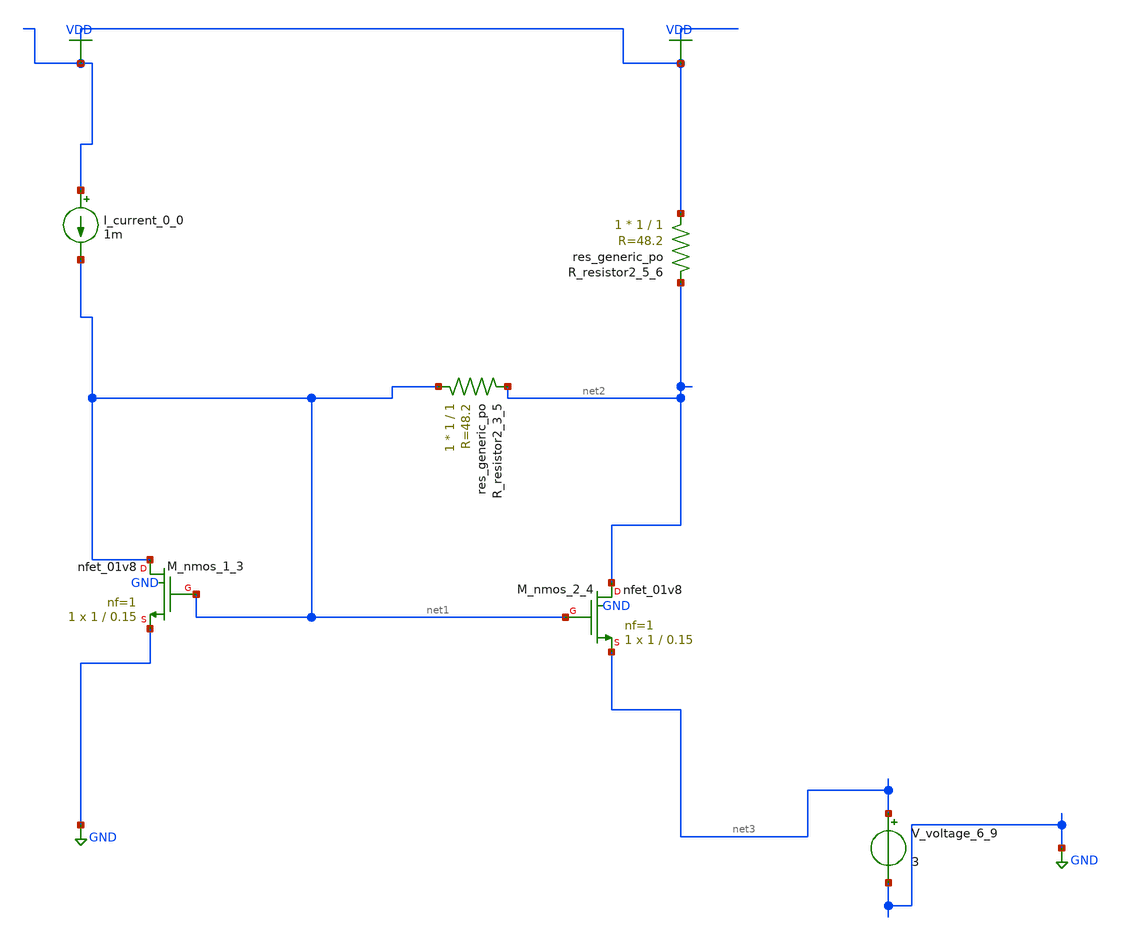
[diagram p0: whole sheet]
** sch_path: schematics/AMSNet/330.sch
**.subckt 330
I_current_0_0 VDD net1 1m
XM_nmos_1_3 net1 net1 GND GND sky130_fd_pr__nfet_01v8 L=0.15 W=1 nf=1 ad='int((1 + 1)/2) * 1 / 1 * 0.29'
+ as='int((1 + 2)/2) * 1 / 1 * 0.29' pd='2*int((1 + 1)/2) * (1 / 1 + 0.29)' ps='2*int((1 + 2)/2) * (1 / 1 + 0.29)'
+ nrd='0.29 / 1 ' nrs='0.29 / 1 ' sa=0 sb=0 sd=0 mult=1 m=1
XM_nmos_2_4 net2 net1 net3 GND sky130_fd_pr__nfet_01v8 L=0.15 W=1 nf=1 ad='int((1 + 1)/2) * 1 / 1 * 0.29'
+ as='int((1 + 2)/2) * 1 / 1 * 0.29' pd='2*int((1 + 1)/2) * (1 / 1 + 0.29)' ps='2*int((1 + 2)/2) * (1 / 1 + 0.29)'
+ nrd='0.29 / 1 ' nrs='0.29 / 1 ' sa=0 sb=0 sd=0 mult=1 m=1
XR_resistor2_3_5 net1 net2 sky130_fd_pr__res_generic_po W=1 L=1 m=1
XR_resistor2_5_6 VDD net2 sky130_fd_pr__res_generic_po W=1 L=1 m=1
V_voltage_6_9 net3 GND 3
**.ends
.GLOBAL GND
.GLOBAL VDD
.end
